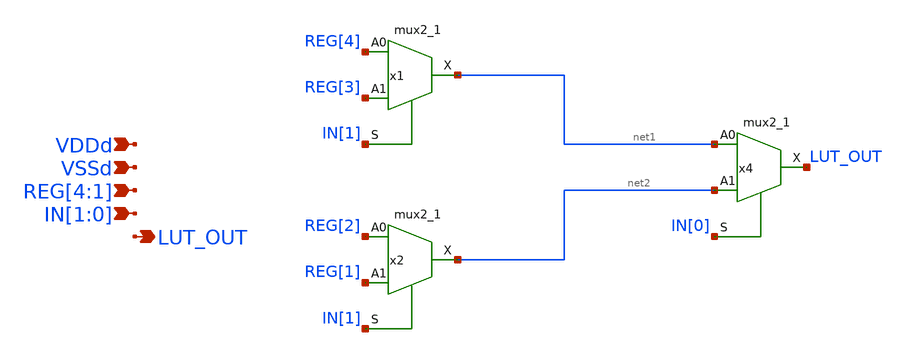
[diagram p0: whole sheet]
** sch_path: designs/libs/core_fpga/LUT/LUT.sch
**.subckt LUT REG[4],REG[3],REG[2],REG[1] IN[1],IN[0] LUT_OUT VDDd VSSd
*.ipin REG[4],REG[3],REG[2],REG[1]
*.ipin IN[1],IN[0]
*.opin LUT_OUT
*.ipin VDDd
*.ipin VSSd
x1 REG[4] REG[3] IN[1] VSSd VDDd VSSd VDDd net1 gf180mcu_fd_sc_mcu9t5v0__mux2_1
x2 REG[2] REG[1] IN[1] VSSd VDDd VSSd VDDd net2 gf180mcu_fd_sc_mcu9t5v0__mux2_1
x4 net1 net2 IN[0] VSSd VDDd VSSd VDDd LUT_OUT gf180mcu_fd_sc_mcu9t5v0__mux2_1
**.ends
.end
